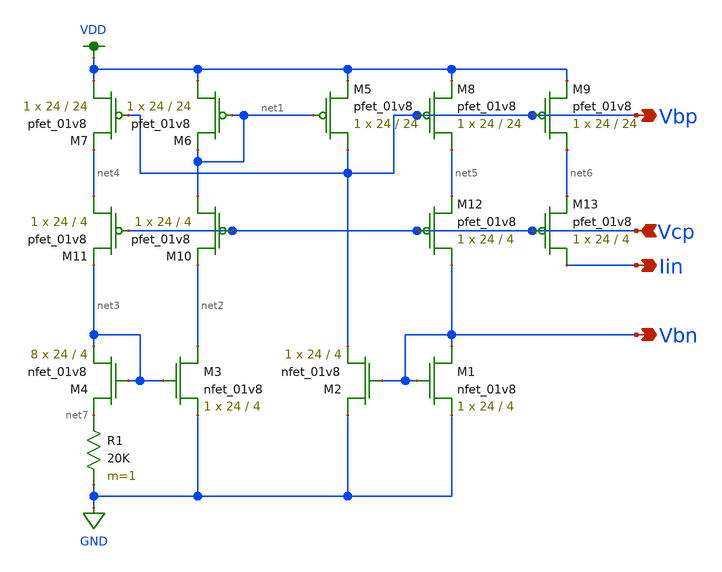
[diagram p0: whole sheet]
** sch_path: xschem/biasGen.sch
**.subckt biasGen Iin Vbp Vbn Vcp
*.opin Iin
*.opin Vbp
*.opin Vbn
*.ipin Vcp
XM1 Vbn Vbn GND GND sky130_fd_pr__nfet_01v8 L=4 W=24 nf=1 ad='int((nf+1)/2) * W/nf * 0.29' as='int((nf+2)/2) * W/nf * 0.29'
+ pd='2*int((nf+1)/2) * (W/nf + 0.29)' ps='2*int((nf+2)/2) * (W/nf + 0.29)' nrd='0.29 / W' nrs='0.29 / W'
+ sa=0 sb=0 sd=0 mult=1 m=1
XM2 GND Vbn Vbp GND sky130_fd_pr__nfet_01v8 L=4 W=24 nf=1 ad='int((nf+1)/2) * W/nf * 0.29' as='int((nf+2)/2) * W/nf * 0.29'
+ pd='2*int((nf+1)/2) * (W/nf + 0.29)' ps='2*int((nf+2)/2) * (W/nf + 0.29)' nrd='0.29 / W' nrs='0.29 / W'
+ sa=0 sb=0 sd=0 mult=1 m=1
XM3 net2 net3 GND GND sky130_fd_pr__nfet_01v8 L=4 W=24 nf=1 ad='int((nf+1)/2) * W/nf * 0.29' as='int((nf+2)/2) * W/nf * 0.29'
+ pd='2*int((nf+1)/2) * (W/nf + 0.29)' ps='2*int((nf+2)/2) * (W/nf + 0.29)' nrd='0.29 / W' nrs='0.29 / W'
+ sa=0 sb=0 sd=0 mult=1 m=1
XM4 net7 net3 net3 GND sky130_fd_pr__nfet_01v8 L=4 W=24 nf=1 ad='int((nf+1)/2) * W/nf * 0.29' as='int((nf+2)/2) * W/nf * 0.29'
+ pd='2*int((nf+1)/2) * (W/nf + 0.29)' ps='2*int((nf+2)/2) * (W/nf + 0.29)' nrd='0.29 / W' nrs='0.29 / W'
+ sa=0 sb=0 sd=0 mult=8 m=8
XM5 Vbp net1 VDD VDD sky130_fd_pr__pfet_01v8 L=24 W=24 nf=1 ad='int((nf+1)/2) * W/nf * 0.29' as='int((nf+2)/2) * W/nf * 0.29'
+ pd='2*int((nf+1)/2) * (W/nf + 0.29)' ps='2*int((nf+2)/2) * (W/nf + 0.29)' nrd='0.29 / W' nrs='0.29 / W'
+ sa=0 sb=0 sd=0 mult=1 m=1
XM6 VDD net1 net1 VDD sky130_fd_pr__pfet_01v8 L=24 W=24 nf=1 ad='int((nf+1)/2) * W/nf * 0.29' as='int((nf+2)/2) * W/nf * 0.29'
+ pd='2*int((nf+1)/2) * (W/nf + 0.29)' ps='2*int((nf+2)/2) * (W/nf + 0.29)' nrd='0.29 / W' nrs='0.29 / W'
+ sa=0 sb=0 sd=0 mult=1 m=1
XM7 VDD Vbp net4 VDD sky130_fd_pr__pfet_01v8 L=24 W=24 nf=1 ad='int((nf+1)/2) * W/nf * 0.29' as='int((nf+2)/2) * W/nf * 0.29'
+ pd='2*int((nf+1)/2) * (W/nf + 0.29)' ps='2*int((nf+2)/2) * (W/nf + 0.29)' nrd='0.29 / W' nrs='0.29 / W'
+ sa=0 sb=0 sd=0 mult=1 m=1
XM8 net5 Vbp VDD VDD sky130_fd_pr__pfet_01v8 L=24 W=24 nf=1 ad='int((nf+1)/2) * W/nf * 0.29' as='int((nf+2)/2) * W/nf * 0.29'
+ pd='2*int((nf+1)/2) * (W/nf + 0.29)' ps='2*int((nf+2)/2) * (W/nf + 0.29)' nrd='0.29 / W' nrs='0.29 / W'
+ sa=0 sb=0 sd=0 mult=1 m=1
R1 net7 GND 20K m=1
XM9 net6 Vbp VDD VDD sky130_fd_pr__pfet_01v8 L=24 W=24 nf=1 ad='int((nf+1)/2) * W/nf * 0.29' as='int((nf+2)/2) * W/nf * 0.29'
+ pd='2*int((nf+1)/2) * (W/nf + 0.29)' ps='2*int((nf+2)/2) * (W/nf + 0.29)' nrd='0.29 / W' nrs='0.29 / W'
+ sa=0 sb=0 sd=0 mult=1 m=1
XM10 net1 Vcp net2 VDD sky130_fd_pr__pfet_01v8 L=4 W=24 nf=1 ad='int((nf+1)/2) * W/nf * 0.29' as='int((nf+2)/2) * W/nf * 0.29'
+ pd='2*int((nf+1)/2) * (W/nf + 0.29)' ps='2*int((nf+2)/2) * (W/nf + 0.29)' nrd='0.29 / W' nrs='0.29 / W'
+ sa=0 sb=0 sd=0 mult=1 m=1
XM11 net4 Vcp net3 VDD sky130_fd_pr__pfet_01v8 L=4 W=24 nf=1 ad='int((nf+1)/2) * W/nf * 0.29' as='int((nf+2)/2) * W/nf * 0.29'
+ pd='2*int((nf+1)/2) * (W/nf + 0.29)' ps='2*int((nf+2)/2) * (W/nf + 0.29)' nrd='0.29 / W' nrs='0.29 / W'
+ sa=0 sb=0 sd=0 mult=1 m=1
XM12 Vbn Vcp net5 VDD sky130_fd_pr__pfet_01v8 L=4 W=24 nf=1 ad='int((nf+1)/2) * W/nf * 0.29' as='int((nf+2)/2) * W/nf * 0.29'
+ pd='2*int((nf+1)/2) * (W/nf + 0.29)' ps='2*int((nf+2)/2) * (W/nf + 0.29)' nrd='0.29 / W' nrs='0.29 / W'
+ sa=0 sb=0 sd=0 mult=1 m=1
XM13 Iin Vcp net6 VDD sky130_fd_pr__pfet_01v8 L=4 W=24 nf=1 ad='int((nf+1)/2) * W/nf * 0.29' as='int((nf+2)/2) * W/nf * 0.29'
+ pd='2*int((nf+1)/2) * (W/nf + 0.29)' ps='2*int((nf+2)/2) * (W/nf + 0.29)' nrd='0.29 / W' nrs='0.29 / W'
+ sa=0 sb=0 sd=0 mult=1 m=1
**.ends
.GLOBAL GND
.GLOBAL VDD
.end
